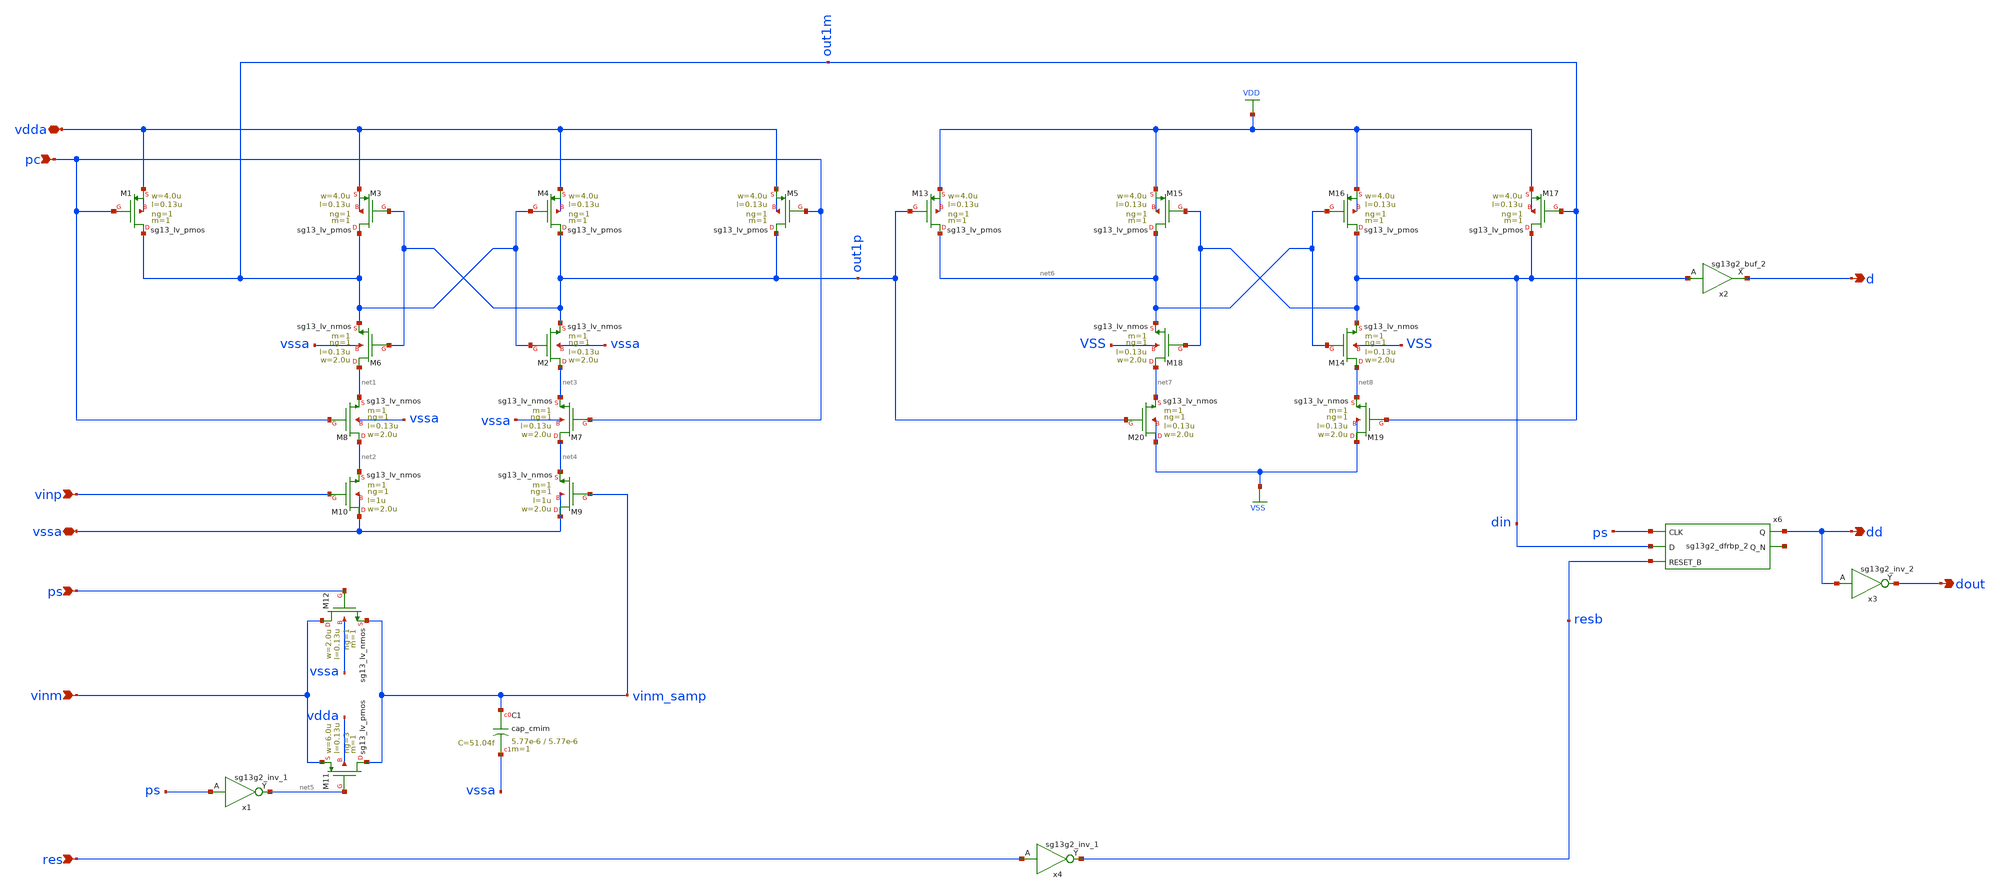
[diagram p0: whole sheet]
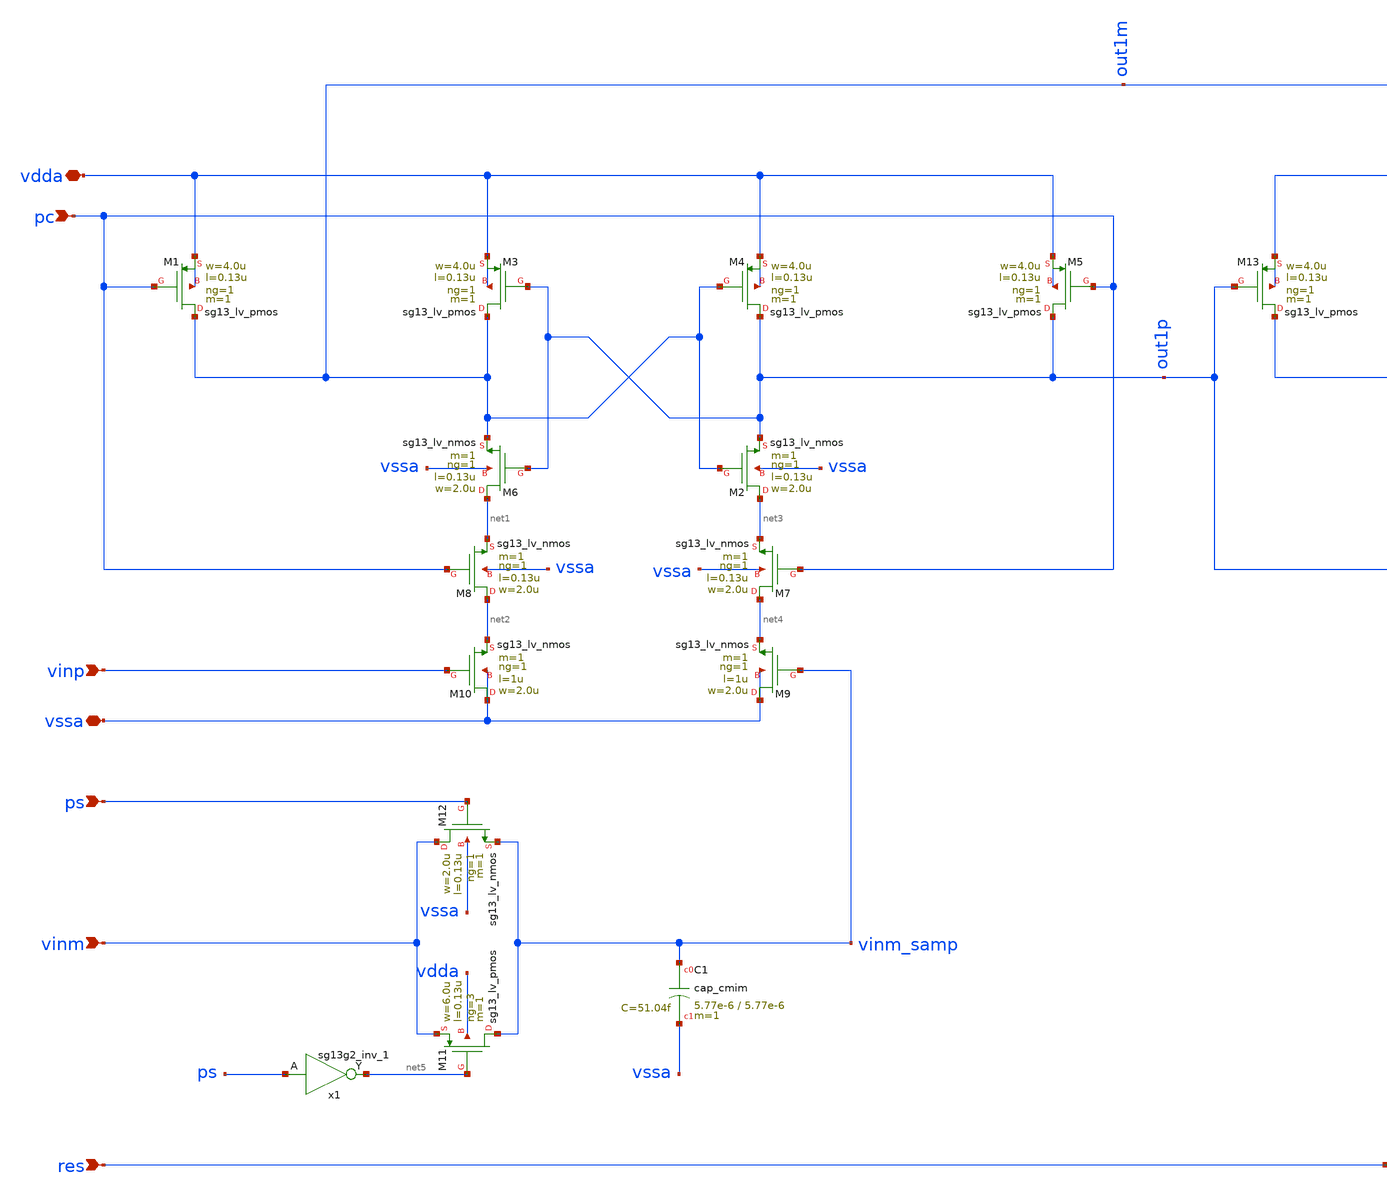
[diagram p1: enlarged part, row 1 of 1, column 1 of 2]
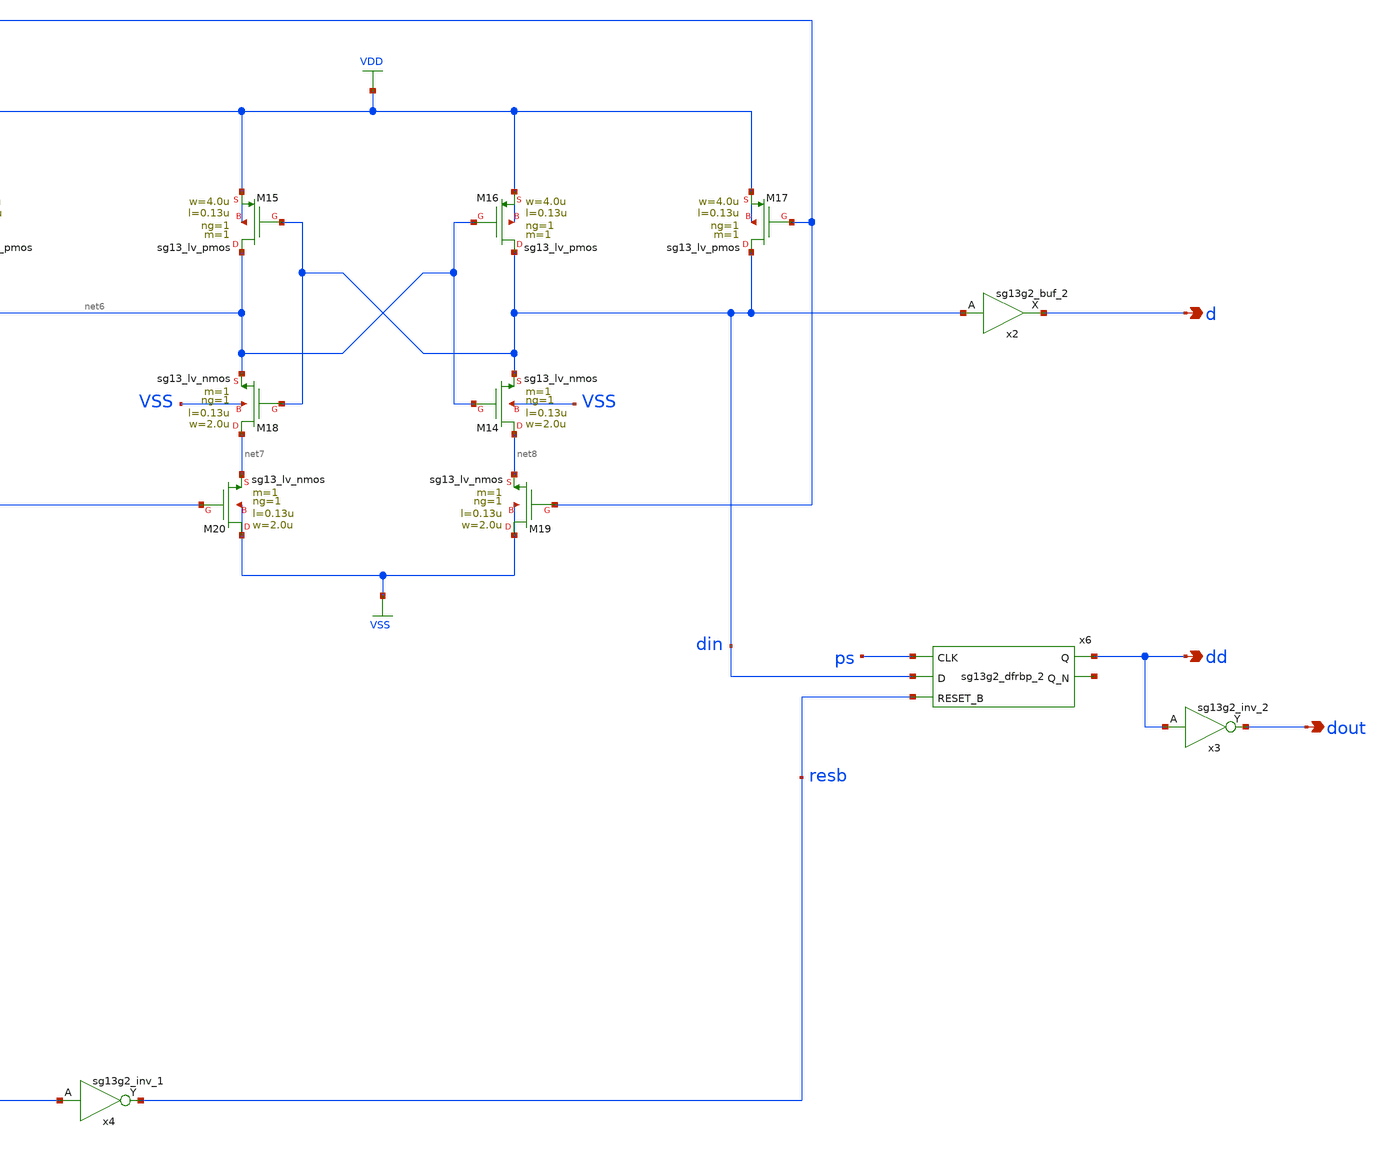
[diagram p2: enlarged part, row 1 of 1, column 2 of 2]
** sch_path: 5_Design/4_Layout/Team 6/xschem/comparator_T6.sch
* IHP-GmbH/IHP-Open-PDK/ihp-sg13g2/libs.tech/xschem/sg13g2_stdcells/sg13g2_inv_2.sch:
* Copyright 2023 IHP PDK Authors
* Licensed under the Apache License, Version 2.0 (the "License");
**.subckt comparator_T6 pc d vdda vinp vssa ps vinm res dd dout
*.ipin pc
*.opin d
*.iopin vdda
*.ipin vinp
*.iopin vssa
*.ipin ps
*.ipin vinm
*.ipin res
*.opin dd
*.opin dout
x1 net5 ps VDD VSS sg13g2_inv_1
x2 d din VDD VSS sg13g2_buf_2
XC1 vinm_samp vssa cap_cmim w=5.77e-6 l=5.77e-6 m=1 mm_ok=1
XM1 out1m pc vdda vdda sg13_lv_pmos w=4.0u l=0.13u ng=1 m=1 mm_ok=1
XM2 net3 out1m out1p vssa sg13_lv_nmos w=2.0u l=0.13u ng=1 m=1 mm_ok=1
XM3 out1m out1p vdda vdda sg13_lv_pmos w=4.0u l=0.13u ng=1 m=1 mm_ok=1
XM4 out1p out1m vdda vdda sg13_lv_pmos w=4.0u l=0.13u ng=1 m=1 mm_ok=1
XM5 out1p pc vdda vdda sg13_lv_pmos w=4.0u l=0.13u ng=1 m=1 mm_ok=1
XM6 net1 out1p out1m vssa sg13_lv_nmos w=2.0u l=0.13u ng=1 m=1 mm_ok=1
XM7 net4 pc net3 vssa sg13_lv_nmos w=2.0u l=0.13u ng=1 m=1 mm_ok=1
XM8 net2 pc net1 vssa sg13_lv_nmos w=2.0u l=0.13u ng=1 m=1 mm_ok=1
XM9 vssa vinm_samp net4 vssa sg13_lv_nmos w=2.0u l=1u ng=1 m=1 mm_ok=1
XM10 vssa vinp net2 vssa sg13_lv_nmos w=2.0u l=1u ng=1 m=1 mm_ok=1
XM11 vinm_samp net5 vinm vdda sg13_lv_pmos w=6.0u l=0.13u ng=3 m=1 mm_ok=1
XM12 vinm ps vinm_samp vssa sg13_lv_nmos w=2.0u l=0.13u ng=1 m=1 mm_ok=1
XM13 net6 out1p VDD VDD sg13_lv_pmos w=4.0u l=0.13u ng=1 m=1 mm_ok=1
XM14 net8 net6 din VSS sg13_lv_nmos w=2.0u l=0.13u ng=1 m=1 mm_ok=1
XM15 net6 din VDD VDD sg13_lv_pmos w=4.0u l=0.13u ng=1 m=1 mm_ok=1
XM16 din net6 VDD VDD sg13_lv_pmos w=4.0u l=0.13u ng=1 m=1 mm_ok=1
XM17 din out1m VDD VDD sg13_lv_pmos w=4.0u l=0.13u ng=1 m=1 mm_ok=1
XM18 net7 din net6 VSS sg13_lv_nmos w=2.0u l=0.13u ng=1 m=1 mm_ok=1
XM19 VSS out1m net8 VSS sg13_lv_nmos w=2.0u l=0.13u ng=1 m=1 mm_ok=1
XM20 VSS out1p net7 VSS sg13_lv_nmos w=2.0u l=0.13u ng=1 m=1 mm_ok=1
x4 resb res VDD VSS sg13g2_inv_1
x3 dout dd VDD VSS sg13g2_inv_2
x6 dd net9 ps din resb VDD VSS sg13g2_dfrbp_2
**.ends

* expanding   symbol:  sg13g2_stdcells/sg13g2_inv_1.sym # of pins=2
** sym_path: sg13g2_stdcells/sg13g2_inv_1.sym
** sch_path: sg13g2_stdcells/sg13g2_inv_1.sch
.subckt sg13g2_inv_1 Y A VDD VSS
*.opin Y
*.ipin A
*.iopin VDD
*.iopin VSS
XM1 Y A VSS VSS sg13_lv_nmos w=740.00n l=130.00n ng=1 m=1 mm_ok=1
XM2 Y A VDD VDD sg13_lv_pmos w=1.12u l=130.00n ng=1 m=1 mm_ok=1
.ends


* expanding   symbol:  sg13g2_stdcells/sg13g2_buf_2.sym # of pins=2
** sym_path: sg13g2_stdcells/sg13g2_buf_2.sym
** sch_path: sg13g2_stdcells/sg13g2_buf_2.sch
.subckt sg13g2_buf_2 X A VDD VSS
*.ipin A
*.opin X
*.iopin VDD
*.iopin VSS
XM1 net1 A VSS VSS sg13_lv_nmos w=640.00n l=130.00n ng=1 m=1 mm_ok=1
XM2 X net1 VSS VSS sg13_lv_nmos w=1.48u l=130.00n ng=2 m=1 mm_ok=1
XM3 net1 A VDD VDD sg13_lv_pmos w=1.000u l=130.00n ng=1 m=1 mm_ok=1
XM4 X net1 VDD VDD sg13_lv_pmos w=2.24u l=130.00n ng=2 m=1 mm_ok=1
.ends


* expanding   symbol:  sg13g2_stdcells/sg13g2_inv_2.sym # of pins=2
** sym_path: sg13g2_stdcells/sg13g2_inv_2.sym
** sch_path: sg13g2_stdcells/sg13g2_inv_2.sch
.subckt sg13g2_inv_2 Y A VDD VSS
*.opin Y
*.ipin A
*.iopin VDD
*.iopin VSS
XM1 Y A VSS VSS sg13_lv_nmos w=1.48u l=130.00n ng=2 m=1 mm_ok=1
XM2 Y A VDD VDD sg13_lv_pmos w=2.24u l=130.00n ng=2 m=1 mm_ok=1
.ends


* expanding   symbol:  sg13g2_stdcells/sg13g2_dfrbp_2.sym # of pins=5
** sym_path: sg13g2_stdcells/sg13g2_dfrbp_2.sym
** sch_path: sg13g2_stdcells/sg13g2_dfrbp_2.sch
.subckt sg13g2_dfrbp_2 Q Q_N CLK D RESET_B VDD VSS
*.ipin D
*.ipin RESET_B
*.ipin CLK
*.opin Q
*.opin Q_N
*.iopin VDD
*.iopin VSS
XM1 Db D net12 VSS sg13_lv_nmos w=420.00n l=130.00n ng=1 m=1 mm_ok=1
XM2 net12 RESET_B VSS VSS sg13_lv_nmos w=420.00n l=130.00n ng=1 m=1 mm_ok=1
XM3 net2 clkneg net11 VSS sg13_lv_nmos w=420.00n l=130.00n ng=1 m=1 mm_ok=1
XM4 net11 net3 VSS VSS sg13_lv_nmos w=420.00n l=130.00n ng=1 m=1 mm_ok=1
XM5 net3 net2 net7 VSS sg13_lv_nmos w=420.00n l=130.00n ng=1 m=1 mm_ok=1
XM6 net7 RESET_B VSS VSS sg13_lv_nmos w=420.00n l=130.00n ng=1 m=1 mm_ok=1
XM7 Q_N net2 VSS VSS sg13_lv_nmos w=1.48u l=130.00n ng=2 m=1 mm_ok=1
XM8 net1 net2 VSS VSS sg13_lv_nmos w=640.00n l=130.00n ng=1 m=1 mm_ok=1
XM9 Q net1 VSS VSS sg13_lv_nmos w=1.48u l=130.00n ng=2 m=1 mm_ok=1
XM10 clkneg CLK VSS VSS sg13_lv_nmos w=740.00n l=130.00n ng=1 m=1 mm_ok=1
XM11 clkpos clkneg VSS VSS sg13_lv_nmos w=740.00n l=130.00n ng=1 m=1 mm_ok=1
XM12 Db clkneg net4 VSS sg13_lv_nmos w=420.00n l=130.00n ng=1 m=1 mm_ok=1
XM13 net4 clkpos net10 VSS sg13_lv_nmos w=420.00n l=130.00n ng=1 m=1 mm_ok=1
XM14 net10 net5 net6 VSS sg13_lv_nmos w=420.00n l=130.00n ng=1 m=1 mm_ok=1
XM15 net6 RESET_B VSS VSS sg13_lv_nmos w=420.00n l=130.00n ng=1 m=1 mm_ok=1
XM16 net5 net4 VSS VSS sg13_lv_nmos w=740.00n l=130.00n ng=1 m=1 mm_ok=1
XM17 net5 clkpos net2 VSS sg13_lv_nmos w=740.00n l=130.00n ng=1 m=1 mm_ok=1
XM18 Db RESET_B VDD VDD sg13_lv_pmos w=420.00n l=130.00n ng=1 m=1 mm_ok=1
XM19 Db D VDD VDD sg13_lv_pmos w=420.00n l=130.00n ng=1 m=1 mm_ok=1
XM20 net9 net3 VDD VDD sg13_lv_pmos w=420.00n l=130.00n ng=1 m=1 mm_ok=1
XM21 net2 clkpos net9 VDD sg13_lv_pmos w=420.00n l=130.00n ng=1 m=1 mm_ok=1
XM22 net3 net2 VDD VDD sg13_lv_pmos w=420.00n l=130.00n ng=1 m=1 mm_ok=1
XM23 net3 RESET_B VDD VDD sg13_lv_pmos w=420.00n l=130.00n ng=1 m=1 mm_ok=1
XM24 Q_N net2 VDD VDD sg13_lv_pmos w=2.24u l=130.00n ng=2 m=1 mm_ok=1
XM25 net1 net2 VDD VDD sg13_lv_pmos w=1.000u l=130.00n ng=1 m=1 mm_ok=1
XM26 Q net1 VDD VDD sg13_lv_pmos w=2.24u l=130.00n ng=2 m=1 mm_ok=1
XM27 clkneg CLK VDD VDD sg13_lv_pmos w=1.12u l=130.00n ng=1 m=1 mm_ok=1
XM28 clkpos clkneg VDD VDD sg13_lv_pmos w=1.12u l=130.00n ng=1 m=1 mm_ok=1
XM29 Db clkpos net4 VDD sg13_lv_pmos w=420.00n l=130.00n ng=1 m=1 mm_ok=1
XM30 net8 net5 VDD VDD sg13_lv_pmos w=420.00n l=130.00n ng=1 m=1 mm_ok=1
XM31 net4 clkneg net8 VDD sg13_lv_pmos w=420.00n l=130.00n ng=1 m=1 mm_ok=1
XM32 net4 RESET_B VDD VDD sg13_lv_pmos w=420.00n l=130.00n ng=1 m=1 mm_ok=1
XM33 net5 net4 VDD VDD sg13_lv_pmos w=1.000u l=130.00n ng=1 m=1 mm_ok=1
XM34 net5 clkneg net2 VDD sg13_lv_pmos w=1.000u l=130.00n ng=1 m=1 mm_ok=1
.ends

.GLOBAL VDD
.GLOBAL VSS
.end
